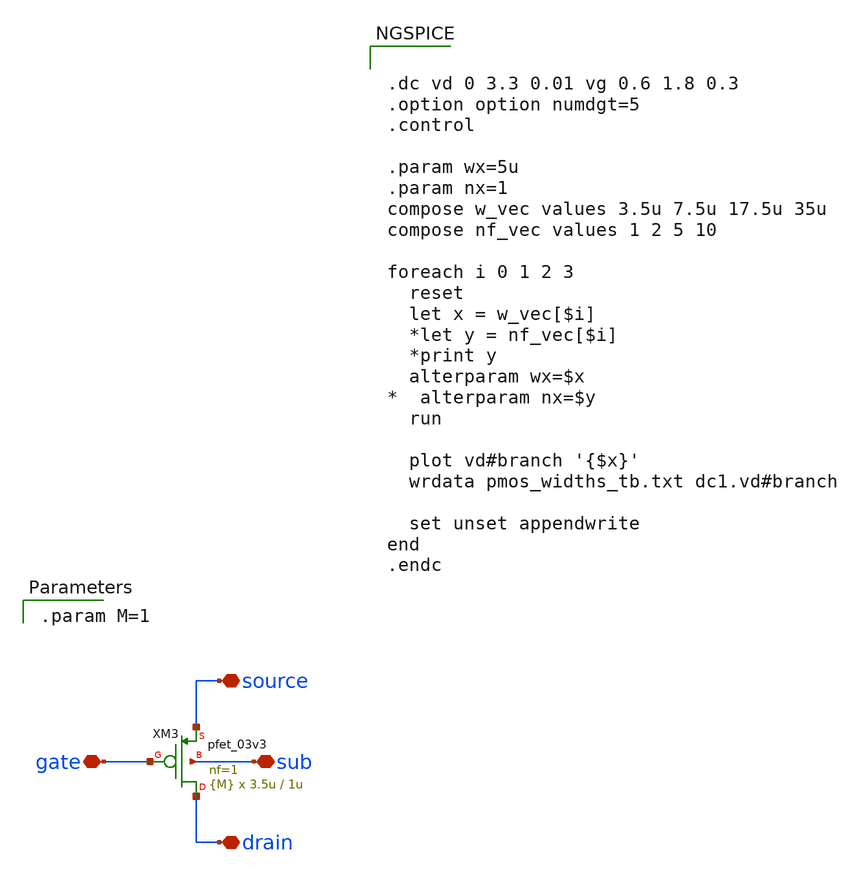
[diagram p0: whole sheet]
** sch_path: designs/switch_matrix_gf180mcu_9t5v0-main/designs/libs/core_analog/unit_pmos/unit_pmos.sch
**.subckt unit_pmos drain source sub gate
*.iopin drain
*.iopin source
*.iopin sub
*.iopin gate
XM3 drain gate source sub pfet_03v3 L=1u W=3.5u nf=1 ad='int((nf+1)/2) * W/nf * 0.18u' as='int((nf+2)/2) * W/nf * 0.18u'
+ pd='2*int((nf+1)/2) * (W/nf + 0.18u)' ps='2*int((nf+2)/2) * (W/nf + 0.18u)' nrd='0.18u / W' nrs='0.18u / W'
+ sa=0 sb=0 sd=0 m={M}
**** begin user architecture code

.param M=1



.dc vd 0 3.3 0.01 vg 0.6 1.8 0.3
.option option numdgt=5
.control

.param wx=5u
.param nx=1
compose w_vec values 3.5u 7.5u 17.5u 35u
compose nf_vec values 1 2 5 10

foreach i 0 1 2 3
  reset
  let x = w_vec[$i]
  *let y = nf_vec[$i]
  *print y
  alterparam wx=$x
*  alterparam nx=$y
  run

  plot vd#branch '{$x}'
  wrdata pmos_widths_tb.txt dc1.vd#branch

  set unset appendwrite
end
.endc


**** end user architecture code
**.ends
.end
